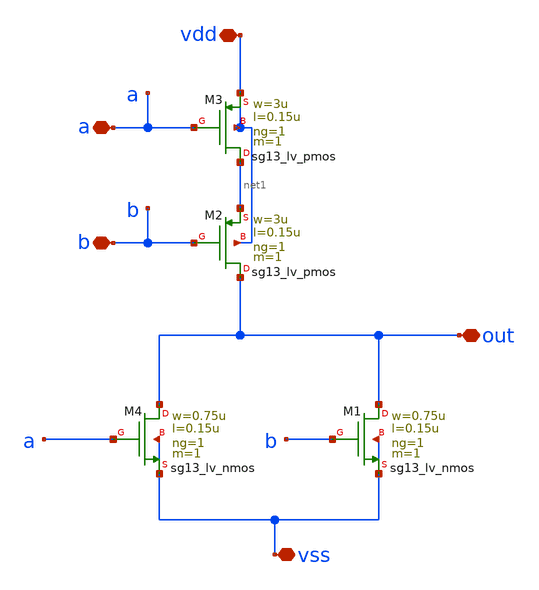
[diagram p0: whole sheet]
** sch_path: design/blocks/norgate/schematic/norgate.sch
**.subckt norgate a vdd b out vss
*.iopin a
*.iopin vdd
*.iopin b
*.iopin out
*.iopin vss
XM1 out b vss vss sg13_lv_nmos w=0.75u l=0.15u ng=1 m=1 mm_ok=1
XM2 out b net1 vdd sg13_lv_pmos w=3u l=0.15u ng=1 m=1 mm_ok=1
XM3 net1 a vdd vdd sg13_lv_pmos w=3u l=0.15u ng=1 m=1 mm_ok=1
XM4 out a vss vss sg13_lv_nmos w=0.75u l=0.15u ng=1 m=1 mm_ok=1
**.ends
.end
